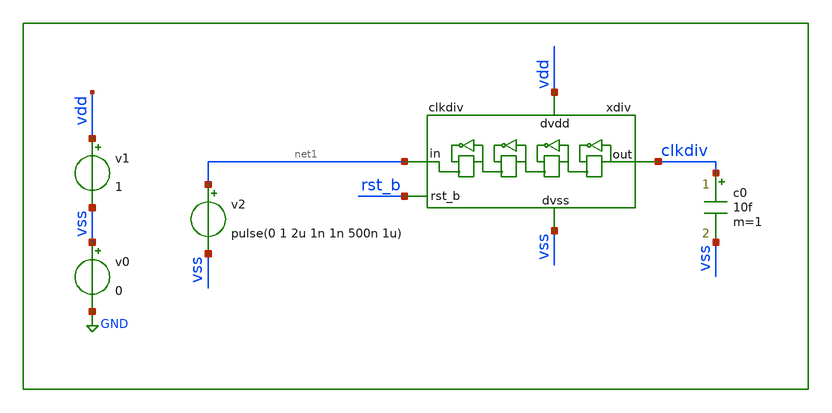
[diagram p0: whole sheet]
** sch_path: xschem/tb/clkdiv/tran_clkdiv.sch
**.subckt tran_clkdiv
v0 vss GND 0
v1 vdd vss 1
c0 clkdiv vss 10f m=1
v2 net1 vss pulse(0 1 2u 1n 1n 500n 1u)
xdiv vss net1 clkdiv rst_b vdd clkdiv
**** begin user architecture code
.options method trap
.option vntol 1e-6

vre  rst_b 0  pulse(0 1 100n 1n 1n 100u 200u)

.control
.param MC_SWITCH=0

tran 1e-9 100e-6
run
.endc


* FET CORNERS
.include $::SKYWATER_MODELS/corners/tt.spice
*.include $::SKYWATER_MODELS/corners/ff.spice
*.include $::SKYWATER_MODELS/corners/ss.spice
*.include $::SKYWATER_MODELS/corners/sf.spice
*.include $::SKYWATER_MODELS/corners/fs.spice

* TT + R + C
*.include $::SKYWATER_MODELS/corners/tt_rmax_cmax.spice
*.include $::SKYWATER_MODELS/corners/tt_rmin_cmin.spice
*.include $::SKYWATER_MODELS/corners/tt_rmax_cmin.spice
*.include $::SKYWATER_MODELS/corners/tt_rmin_cmax.spice

* FF + R + C
*.include $::SKYWATER_MODELS/corners/ff_rmax_cmax.spice
*.include $::SKYWATER_MODELS/corners/ff_rmin_cmin.spice
*.include $::SKYWATER_MODELS/corners/ff_rmax_cmin.spice
*.include $::SKYWATER_MODELS/corners/ff_rmin_cmax.spice


* SS + R + C
*.include $::SKYWATER_MODELS/corners/ss_rmax_cmax.spice
*.include $::SKYWATER_MODELS/corners/ss_rmin_cmin.spice
*.include $::SKYWATER_MODELS/corners/ss_rmax_cmin.spice
*.include $::SKYWATER_MODELS/corners/ss_rmin_cmax.spice

* SF + R + C
*.include $::SKYWATER_MODELS/corners/sf_rmax_cmax.spice
*.include $::SKYWATER_MODELS/corners/sf_rmin_cmin.spice
*.include $::SKYWATER_MODELS/corners/sf_rmax_cmin.spice
*.include $::SKYWATER_MODELS/corners/sf_rmin_cmax.spice

* FS + R + C
*.include $::SKYWATER_MODELS/corners/fs_rmax_cmax.spice
*.include $::SKYWATER_MODELS/corners/fs_rmin_cmin.spice
*.include $::SKYWATER_MODELS/corners/fs_rmax_cmin.spice
*.include $::SKYWATER_MODELS/corners/fs_rmin_cmax.spice

**** end user architecture code
**.ends

* expanding   symbol:  clkdiv/clkdiv.sym # of pins=5
** sym_path: xschem/clkdiv/clkdiv.sym
** sch_path: xschem/clkdiv/clkdiv.sch
.subckt clkdiv dvss in out rst_b dvdd
*.ipin in
*.ipin rst_b
*.opin out
*.iopin dvdd
*.iopin dvss
x6 in net1 rst_b dvss dvss dvdd dvdd div2 net5 sky130_fd_sc_hd__dfrbp_1
x8 div2 dvss dvss dvdd dvdd net1 sky130_fd_sc_hd__inv_1
* noconn #net5
x1 div2 net2 rst_b dvss dvss dvdd dvdd div4 net6 sky130_fd_sc_hd__dfrbp_1
x2 div4 dvss dvss dvdd dvdd net2 sky130_fd_sc_hd__inv_1
* noconn #net6
x3 div4 net3 rst_b dvss dvss dvdd dvdd div8 net7 sky130_fd_sc_hd__dfrbp_1
x4 div8 dvss dvss dvdd dvdd net3 sky130_fd_sc_hd__inv_1
* noconn #net7
x5 div8 net4 rst_b dvss dvss dvdd dvdd out net8 sky130_fd_sc_hd__dfrbp_1
x7 out dvss dvss dvdd dvdd net4 sky130_fd_sc_hd__inv_1
* noconn #net8
xdec[7] dvss dvss dvdd dvdd sky130_fd_sc_hd__decap_4
xdec[6] dvss dvss dvdd dvdd sky130_fd_sc_hd__decap_4
xdec[5] dvss dvss dvdd dvdd sky130_fd_sc_hd__decap_4
xdec[4] dvss dvss dvdd dvdd sky130_fd_sc_hd__decap_4
xdec[3] dvss dvss dvdd dvdd sky130_fd_sc_hd__decap_4
xdec[2] dvss dvss dvdd dvdd sky130_fd_sc_hd__decap_4
xdec[1] dvss dvss dvdd dvdd sky130_fd_sc_hd__decap_4
xdec[0] dvss dvss dvdd dvdd sky130_fd_sc_hd__decap_4
xtap dvss dvdd sky130_fd_sc_hd__tapvpwrvgnd_1
.ends

.GLOBAL GND
**** begin user architecture code
[sky130_models]

**** end user architecture code
.end
